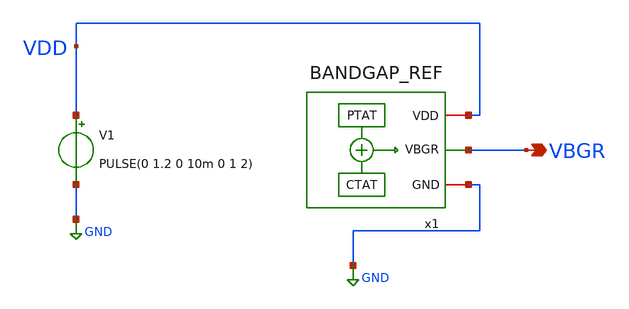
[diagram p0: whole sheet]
** sch_path: xschem/bgr/tb_BGR_PEX.sch
**.subckt tb_BGR_PEX VBGR
*.opin VBGR
V1 VDD GND PULSE(0 1.2 0 10m 0 1 2)
x1 VDD GND VBGR BANDGAP_REF_PEX
**** begin user architecture code



.option rshunt=1.0e12
.control
save all
save VDD
alter V1 dc 1.2

op
print I(Vmeas)
print v(VBGR)
print -i(V1)

dc TEMP 100 -50 -5
print I(Vmeas)
print v(VBGR)
plot v(VBGR)

write tb_BGR_PEX_temp.raw
.endc

.control
save all
tran 100u 15m

print I(Vmeas)
meas tran vb_end find v(VBGR) at=15m
meas tran vb_max max v(VBGR) from=5m to=15m
meas tran vb_min min v(VBGR) from=5m to=15m
* supply current (negative = drawn from the source), power = 1.2 V x |idd|
meas tran idd avg i(V1) from=13m to=15m
plot v(VBGR)

write tb_BGR_PEX_transient.raw
.endc




.include /foss/designs/unicasss-tools/SG13G2_2.4GHz_LC_VCO_FPLL/pex/BANDGAP_REF__BANDGAP_REF/magic_RC/BANDGAP_REF.pex.spice
.lib cornerMOSlv.lib mos_tt
.lib cornerMOShv.lib mos_tt
.lib cornerRES.lib res_typ
.lib cornerCAP.lib cap_typ

**** end user architecture code
**.ends
.GLOBAL GND
.end
